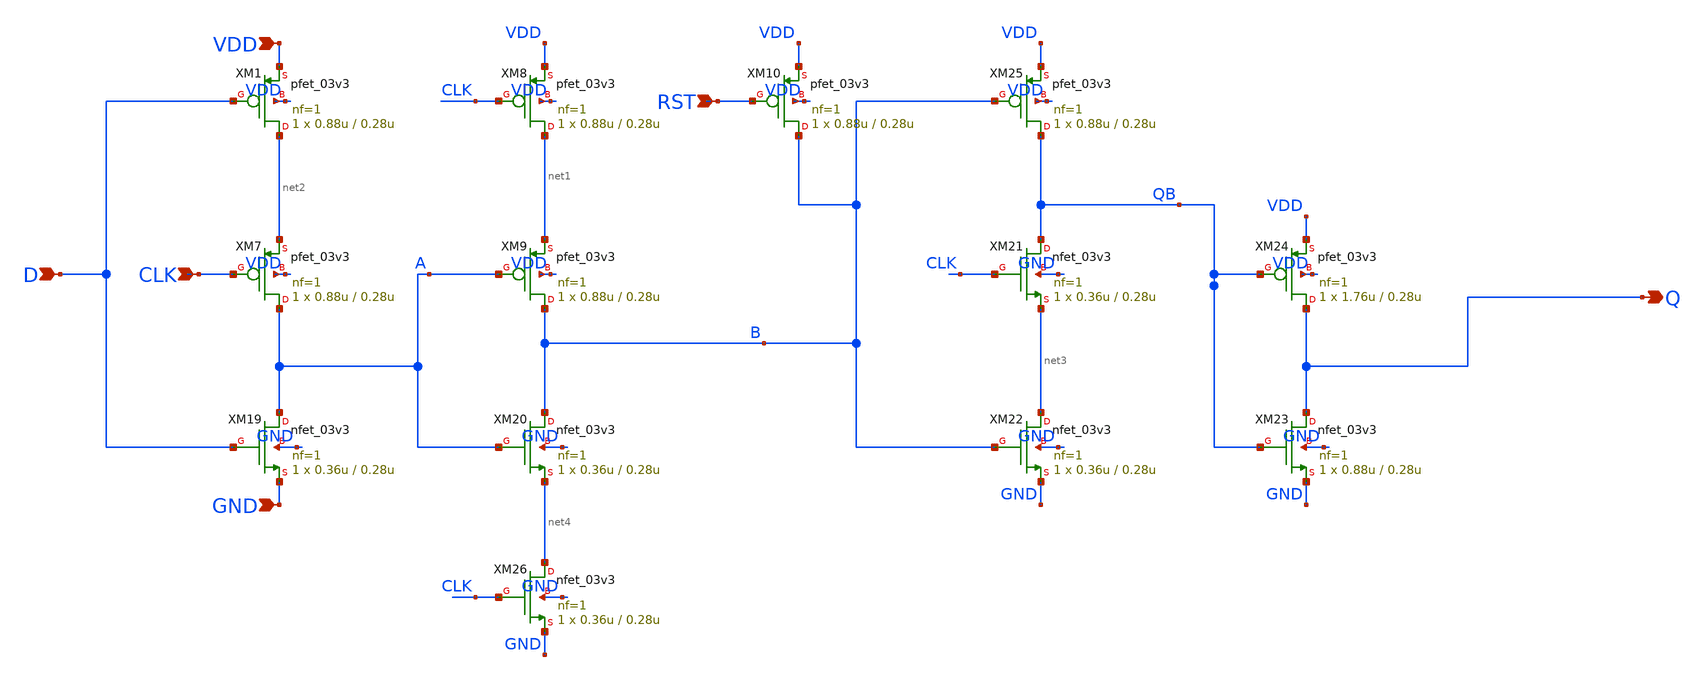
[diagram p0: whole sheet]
** sch_path: blocks/adc/encoder/sym/dff_encoder.sch
**.subckt dff_encoder Q D CLK RST VDD GND
*.opin Q
*.ipin D
*.ipin CLK
*.ipin RST
*.ipin VDD
*.ipin GND
XM1 net2 D VDD VDD pfet_03v3 L=0.28u W=0.88u nf=1 ad='int((nf+1)/2) * W/nf * 0.18u' as='int((nf+2)/2) * W/nf * 0.18u'
+ pd='2*int((nf+1)/2) * (W/nf + 0.18u)' ps='2*int((nf+2)/2) * (W/nf + 0.18u)' nrd='0.18u / W' nrs='0.18u / W'
+ sa=0 sb=0 sd=0 m=1
XM7 A CLK net2 VDD pfet_03v3 L=0.28u W=0.88u nf=1 ad='int((nf+1)/2) * W/nf * 0.18u' as='int((nf+2)/2) * W/nf * 0.18u'
+ pd='2*int((nf+1)/2) * (W/nf + 0.18u)' ps='2*int((nf+2)/2) * (W/nf + 0.18u)' nrd='0.18u / W' nrs='0.18u / W'
+ sa=0 sb=0 sd=0 m=1
XM8 net1 CLK VDD VDD pfet_03v3 L=0.28u W=0.88u nf=1 ad='int((nf+1)/2) * W/nf * 0.18u' as='int((nf+2)/2) * W/nf * 0.18u'
+ pd='2*int((nf+1)/2) * (W/nf + 0.18u)' ps='2*int((nf+2)/2) * (W/nf + 0.18u)' nrd='0.18u / W' nrs='0.18u / W'
+ sa=0 sb=0 sd=0 m=1
XM9 B A net1 VDD pfet_03v3 L=0.28u W=0.88u nf=1 ad='int((nf+1)/2) * W/nf * 0.18u' as='int((nf+2)/2) * W/nf * 0.18u'
+ pd='2*int((nf+1)/2) * (W/nf + 0.18u)' ps='2*int((nf+2)/2) * (W/nf + 0.18u)' nrd='0.18u / W' nrs='0.18u / W'
+ sa=0 sb=0 sd=0 m=1
XM10 B RST VDD VDD pfet_03v3 L=0.28u W=0.88u nf=1 ad='int((nf+1)/2) * W/nf * 0.18u' as='int((nf+2)/2) * W/nf * 0.18u'
+ pd='2*int((nf+1)/2) * (W/nf + 0.18u)' ps='2*int((nf+2)/2) * (W/nf + 0.18u)' nrd='0.18u / W' nrs='0.18u / W'
+ sa=0 sb=0 sd=0 m=1
XM19 A D GND GND nfet_03v3 L=0.28u W=0.36u nf=1 ad='int((nf+1)/2) * W/nf * 0.18u' as='int((nf+2)/2) * W/nf * 0.18u'
+ pd='2*int((nf+1)/2) * (W/nf + 0.18u)' ps='2*int((nf+2)/2) * (W/nf + 0.18u)' nrd='0.18u / W' nrs='0.18u / W'
+ sa=0 sb=0 sd=0 m=1
XM20 B A net4 GND nfet_03v3 L=0.28u W=0.36u nf=1 ad='int((nf+1)/2) * W/nf * 0.18u' as='int((nf+2)/2) * W/nf * 0.18u'
+ pd='2*int((nf+1)/2) * (W/nf + 0.18u)' ps='2*int((nf+2)/2) * (W/nf + 0.18u)' nrd='0.18u / W' nrs='0.18u / W'
+ sa=0 sb=0 sd=0 m=1
XM21 QB CLK net3 GND nfet_03v3 L=0.28u W=0.36u nf=1 ad='int((nf+1)/2) * W/nf * 0.18u' as='int((nf+2)/2) * W/nf * 0.18u'
+ pd='2*int((nf+1)/2) * (W/nf + 0.18u)' ps='2*int((nf+2)/2) * (W/nf + 0.18u)' nrd='0.18u / W' nrs='0.18u / W'
+ sa=0 sb=0 sd=0 m=1
XM22 net3 B GND GND nfet_03v3 L=0.28u W=0.36u nf=1 ad='int((nf+1)/2) * W/nf * 0.18u' as='int((nf+2)/2) * W/nf * 0.18u'
+ pd='2*int((nf+1)/2) * (W/nf + 0.18u)' ps='2*int((nf+2)/2) * (W/nf + 0.18u)' nrd='0.18u / W' nrs='0.18u / W'
+ sa=0 sb=0 sd=0 m=1
XM23 Q QB GND GND nfet_03v3 L=0.28u W=0.88u nf=1 ad='int((nf+1)/2) * W/nf * 0.18u' as='int((nf+2)/2) * W/nf * 0.18u'
+ pd='2*int((nf+1)/2) * (W/nf + 0.18u)' ps='2*int((nf+2)/2) * (W/nf + 0.18u)' nrd='0.18u / W' nrs='0.18u / W'
+ sa=0 sb=0 sd=0 m=1
XM24 Q QB VDD VDD pfet_03v3 L=0.28u W=1.76u nf=1 ad='int((nf+1)/2) * W/nf * 0.18u' as='int((nf+2)/2) * W/nf * 0.18u'
+ pd='2*int((nf+1)/2) * (W/nf + 0.18u)' ps='2*int((nf+2)/2) * (W/nf + 0.18u)' nrd='0.18u / W' nrs='0.18u / W'
+ sa=0 sb=0 sd=0 m=1
XM25 QB B VDD VDD pfet_03v3 L=0.28u W=0.88u nf=1 ad='int((nf+1)/2) * W/nf * 0.18u' as='int((nf+2)/2) * W/nf * 0.18u'
+ pd='2*int((nf+1)/2) * (W/nf + 0.18u)' ps='2*int((nf+2)/2) * (W/nf + 0.18u)' nrd='0.18u / W' nrs='0.18u / W'
+ sa=0 sb=0 sd=0 m=1
XM26 net4 CLK GND GND nfet_03v3 L=0.28u W=0.36u nf=1 ad='int((nf+1)/2) * W/nf * 0.18u' as='int((nf+2)/2) * W/nf * 0.18u'
+ pd='2*int((nf+1)/2) * (W/nf + 0.18u)' ps='2*int((nf+2)/2) * (W/nf + 0.18u)' nrd='0.18u / W' nrs='0.18u / W'
+ sa=0 sb=0 sd=0 m=1
**.ends
.end
